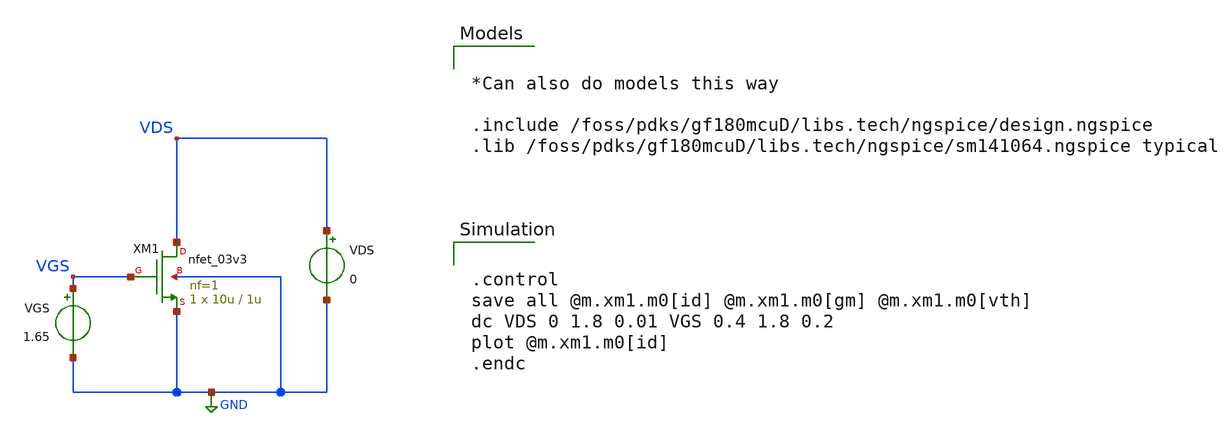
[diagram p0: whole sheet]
** sch_path: designs/sophiazhu/session_1/nmos_id_vds_param.sch
**.subckt nmos_id_vds_param
XM1 VDS VGS GND GND nfet_03v3 L=1u W=10u nf=1 ad='int((nf+1)/2) * W/nf * 0.18u' as='int((nf+2)/2) * W/nf * 0.18u'
+ pd='2*int((nf+1)/2) * (W/nf + 0.18u)' ps='2*int((nf+2)/2) * (W/nf + 0.18u)' nrd='0.18u / W' nrs='0.18u / W'
+ sa=0 sb=0 sd=0 m=1
VDS VDS GND 0
VGS VGS GND 1.65
**** begin user architecture code


.control
save all @m.xm1.m0[id] @m.xm1.m0[gm] @m.xm1.m0[vth]
dc VDS 0 1.8 0.01 VGS 0.4 1.8 0.2
plot @m.xm1.m0[id]
.endc



*Can also do models this way

.include /foss/pdks/gf180mcuD/libs.tech/ngspice/design.ngspice
.lib /foss/pdks/gf180mcuD/libs.tech/ngspice/sm141064.ngspice typical

**** end user architecture code
**.ends
.GLOBAL GND
.end
